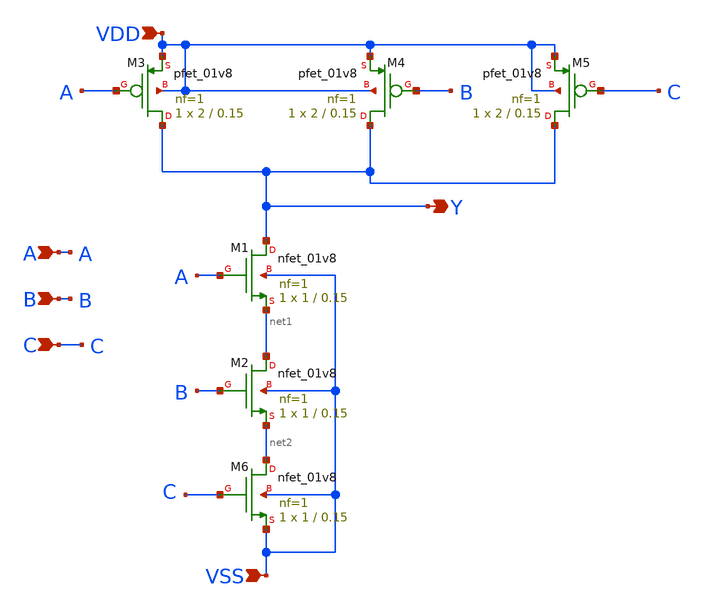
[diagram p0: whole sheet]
** sch_path: nand_FFD_3pin.sch
**.subckt nand_FFD_3pin VDD A B VSS Y C
*.ipin VDD
*.ipin A
*.ipin B
*.ipin VSS
*.opin Y
*.ipin C
XM1 Y A net1 VSS sky130_fd_pr__nfet_01v8 L=0.15 W=1 nf=1 ad='int((nf+1)/2) * W/nf * 0.29' as='int((nf+2)/2) * W/nf * 0.29'
+ pd='2*int((nf+1)/2) * (W/nf + 0.29)' ps='2*int((nf+2)/2) * (W/nf + 0.29)' nrd='0.29 / W' nrs='0.29 / W'
+ sa=0 sb=0 sd=0 mult=1 m=1
XM2 net1 B net2 VSS sky130_fd_pr__nfet_01v8 L=0.15 W=1 nf=1 ad='int((nf+1)/2) * W/nf * 0.29' as='int((nf+2)/2) * W/nf * 0.29'
+ pd='2*int((nf+1)/2) * (W/nf + 0.29)' ps='2*int((nf+2)/2) * (W/nf + 0.29)' nrd='0.29 / W' nrs='0.29 / W'
+ sa=0 sb=0 sd=0 mult=1 m=1
XM3 Y A VDD VDD sky130_fd_pr__pfet_01v8 L=0.15 W=2 nf=1 ad='int((nf+1)/2) * W/nf * 0.29' as='int((nf+2)/2) * W/nf * 0.29'
+ pd='2*int((nf+1)/2) * (W/nf + 0.29)' ps='2*int((nf+2)/2) * (W/nf + 0.29)' nrd='0.29 / W' nrs='0.29 / W'
+ sa=0 sb=0 sd=0 mult=1 m=1
XM4 Y B VDD VDD sky130_fd_pr__pfet_01v8 L=0.15 W=2 nf=1 ad='int((nf+1)/2) * W/nf * 0.29' as='int((nf+2)/2) * W/nf * 0.29'
+ pd='2*int((nf+1)/2) * (W/nf + 0.29)' ps='2*int((nf+2)/2) * (W/nf + 0.29)' nrd='0.29 / W' nrs='0.29 / W'
+ sa=0 sb=0 sd=0 mult=1 m=1
XM5 Y C VDD VDD sky130_fd_pr__pfet_01v8 L=0.15 W=2 nf=1 ad='int((nf+1)/2) * W/nf * 0.29' as='int((nf+2)/2) * W/nf * 0.29'
+ pd='2*int((nf+1)/2) * (W/nf + 0.29)' ps='2*int((nf+2)/2) * (W/nf + 0.29)' nrd='0.29 / W' nrs='0.29 / W'
+ sa=0 sb=0 sd=0 mult=1 m=1
XM6 net2 C VSS VSS sky130_fd_pr__nfet_01v8 L=0.15 W=1 nf=1 ad='int((nf+1)/2) * W/nf * 0.29' as='int((nf+2)/2) * W/nf * 0.29'
+ pd='2*int((nf+1)/2) * (W/nf + 0.29)' ps='2*int((nf+2)/2) * (W/nf + 0.29)' nrd='0.29 / W' nrs='0.29 / W'
+ sa=0 sb=0 sd=0 mult=1 m=1
**.ends
.end
